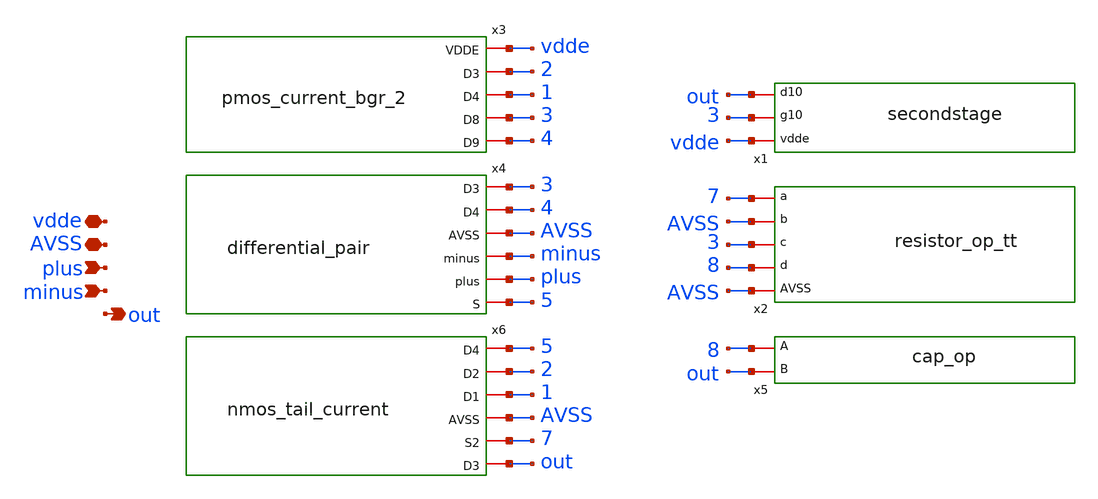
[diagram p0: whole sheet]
** sch_path: magic/op5.sch
**.subckt op5 vdde AVSS plus minus out
*.iopin vdde
*.iopin AVSS
*.ipin plus
*.ipin minus
*.opin out
x1 vdde 3 out secondstage
x2 AVSS 8 3 AVSS 7 resistor_op_tt
x3 vdde 2 1 3 4 pmos_current_bgr_2
x4 3 4 AVSS minus plus 5 differential_pair
x5 out 8 cap_op
x6 5 2 1 AVSS 7 out nmos_tail_current
**.ends
.end
